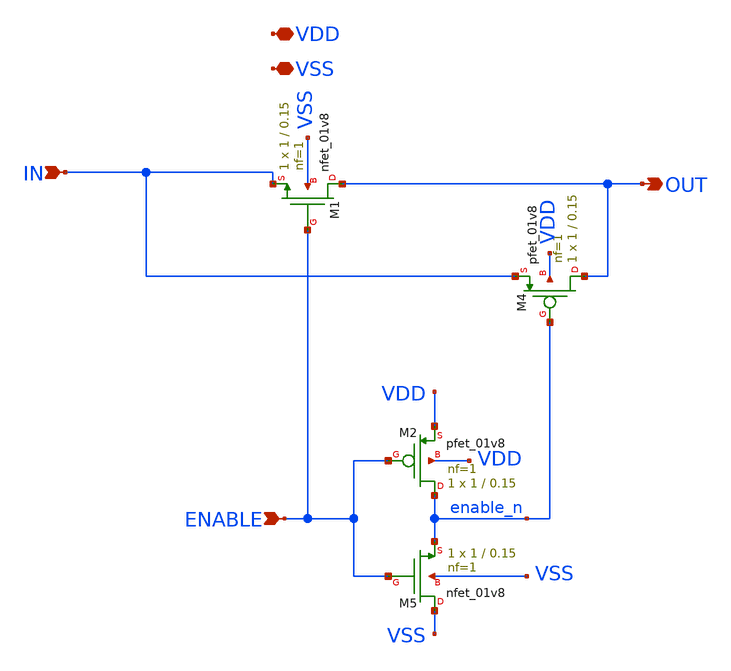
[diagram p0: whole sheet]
** sch_path: xschem/answitch.sch
* (C) 2024 Pat Deegan
* https://psychogenic.com
**.subckt answitch VDD VSS ENABLE OUT IN
*.iopin VDD
*.iopin VSS
*.ipin ENABLE
*.opin OUT
*.ipin IN
XM1 OUT ENABLE IN VSS sky130_fd_pr__nfet_01v8 L=0.15 W=1 nf=1 ad='int((nf+1)/2) * W/nf * 0.29' as='int((nf+2)/2) * W/nf * 0.29'
+ pd='2*int((nf+1)/2) * (W/nf + 0.29)' ps='2*int((nf+2)/2) * (W/nf + 0.29)' nrd='0.29 / W' nrs='0.29 / W'
+ sa=0 sb=0 sd=0 mult=1 m=1
XM5 VSS ENABLE enable_n VSS sky130_fd_pr__nfet_01v8 L=0.15 W=1 nf=1 ad='int((nf+1)/2) * W/nf * 0.29'
+ as='int((nf+2)/2) * W/nf * 0.29' pd='2*int((nf+1)/2) * (W/nf + 0.29)' ps='2*int((nf+2)/2) * (W/nf + 0.29)'
+ nrd='0.29 / W' nrs='0.29 / W' sa=0 sb=0 sd=0 mult=1 m=1
XM2 enable_n ENABLE VDD VDD sky130_fd_pr__pfet_01v8 L=0.15 W=1 nf=1 ad='int((nf+1)/2) * W/nf * 0.29'
+ as='int((nf+2)/2) * W/nf * 0.29' pd='2*int((nf+1)/2) * (W/nf + 0.29)' ps='2*int((nf+2)/2) * (W/nf + 0.29)'
+ nrd='0.29 / W' nrs='0.29 / W' sa=0 sb=0 sd=0 mult=1 m=1
XM4 OUT enable_n IN VDD sky130_fd_pr__pfet_01v8 L=0.15 W=1 nf=1 ad='int((nf+1)/2) * W/nf * 0.29' as='int((nf+2)/2) * W/nf * 0.29'
+ pd='2*int((nf+1)/2) * (W/nf + 0.29)' ps='2*int((nf+2)/2) * (W/nf + 0.29)' nrd='0.29 / W' nrs='0.29 / W'
+ sa=0 sb=0 sd=0 mult=1 m=1
**.ends
.end
